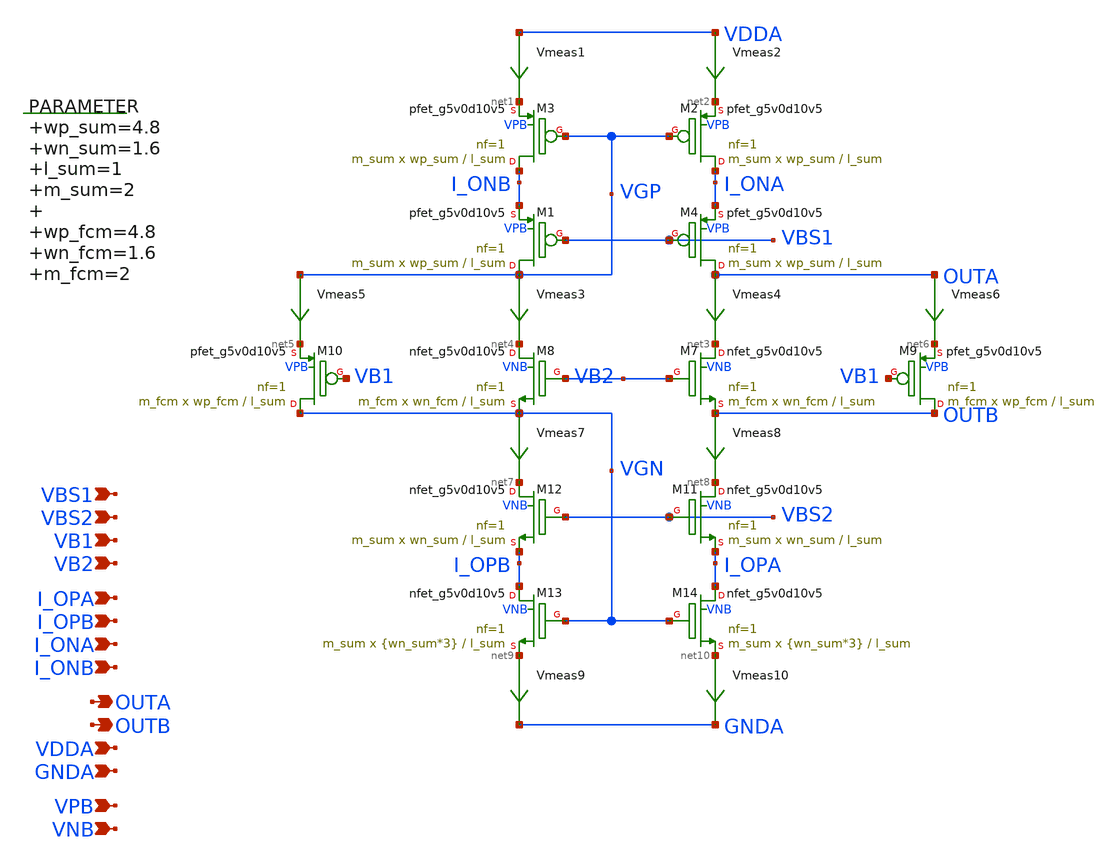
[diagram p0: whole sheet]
** sch_path: xschem/folded_cascode.sch
**.subckt folded_cascode I_OPA I_OPB I_ONA I_ONB OUTA OUTB VBS1 VBS2 VB1 VB2 VDDA VPB GNDA VNB
*.ipin I_OPA
*.ipin I_OPB
*.ipin I_ONA
*.ipin I_ONB
*.opin OUTA
*.opin OUTB
*.ipin VBS1
*.ipin VBS2
*.ipin VB1
*.ipin VB2
*.ipin VDDA
*.ipin VPB
*.ipin GNDA
*.ipin VNB
.param wp_sum=4.8 wn_sum=1.6 l_sum=1 m_sum=2 wp_fcm=4.8 wn_fcm=1.6 m_fcm=2

XM3 I_ONB VGP net1 VPB sky130_fd_pr__pfet_g5v0d10v5 L=l_sum W=wp_sum nf=1 ad='int((nf+1)/2) * W/nf * 0.29'
+ as='int((nf+2)/2) * W/nf * 0.29' pd='2*int((nf+1)/2) * (W/nf + 0.29)' ps='2*int((nf+2)/2) * (W/nf + 0.29)'
+ nrd='0.29 / W' nrs='0.29 / W' sa=0 sb=0 sd=0 mult=m_sum m=m_sum
Vmeas1 VDDA net1 0
.save i(vmeas1)
Vmeas2 VDDA net2 0
.save i(vmeas2)
XM7 net3 VB2 OUTB VNB sky130_fd_pr__nfet_g5v0d10v5 L=l_sum W=wn_fcm nf=1 ad='int((nf+1)/2) * W/nf * 0.29'
+ as='int((nf+2)/2) * W/nf * 0.29' pd='2*int((nf+1)/2) * (W/nf + 0.29)' ps='2*int((nf+2)/2) * (W/nf + 0.29)'
+ nrd='0.29 / W' nrs='0.29 / W' sa=0 sb=0 sd=0 mult=m_fcm m=m_fcm
XM8 net4 VB2 VGN VNB sky130_fd_pr__nfet_g5v0d10v5 L=l_sum W=wn_fcm nf=1 ad='int((nf+1)/2) * W/nf * 0.29'
+ as='int((nf+2)/2) * W/nf * 0.29' pd='2*int((nf+1)/2) * (W/nf + 0.29)' ps='2*int((nf+2)/2) * (W/nf + 0.29)'
+ nrd='0.29 / W' nrs='0.29 / W' sa=0 sb=0 sd=0 mult=m_fcm m=m_fcm
Vmeas3 VGP net4 0
.save i(vmeas3)
Vmeas4 OUTA net3 0
.save i(vmeas4)
XM10 VGN VB1 net5 VPB sky130_fd_pr__pfet_g5v0d10v5 L=l_sum W=wp_fcm nf=1 ad='int((nf+1)/2) * W/nf * 0.29'
+ as='int((nf+2)/2) * W/nf * 0.29' pd='2*int((nf+1)/2) * (W/nf + 0.29)' ps='2*int((nf+2)/2) * (W/nf + 0.29)'
+ nrd='0.29 / W' nrs='0.29 / W' sa=0 sb=0 sd=0 mult=m_fcm m=m_fcm
Vmeas5 VGP net5 0
.save i(vmeas5)
Vmeas6 OUTA net6 0
.save i(vmeas6)
XM9 OUTB VB1 net6 VPB sky130_fd_pr__pfet_g5v0d10v5 L=l_sum W=wp_fcm nf=1 ad='int((nf+1)/2) * W/nf * 0.29'
+ as='int((nf+2)/2) * W/nf * 0.29' pd='2*int((nf+1)/2) * (W/nf + 0.29)' ps='2*int((nf+2)/2) * (W/nf + 0.29)'
+ nrd='0.29 / W' nrs='0.29 / W' sa=0 sb=0 sd=0 mult=m_fcm m=m_fcm
XM12 net7 VBS2 I_OPB VNB sky130_fd_pr__nfet_g5v0d10v5 L=l_sum W=wn_sum nf=1 ad='int((nf+1)/2) * W/nf * 0.29'
+ as='int((nf+2)/2) * W/nf * 0.29' pd='2*int((nf+1)/2) * (W/nf + 0.29)' ps='2*int((nf+2)/2) * (W/nf + 0.29)'
+ nrd='0.29 / W' nrs='0.29 / W' sa=0 sb=0 sd=0 mult=m_sum m=m_sum
Vmeas7 VGN net7 0
.save i(vmeas7)
Vmeas8 OUTB net8 0
.save i(vmeas8)
XM11 net8 VBS2 I_OPA VNB sky130_fd_pr__nfet_g5v0d10v5 L=l_sum W=wn_sum nf=1 ad='int((nf+1)/2) * W/nf * 0.29'
+ as='int((nf+2)/2) * W/nf * 0.29' pd='2*int((nf+1)/2) * (W/nf + 0.29)' ps='2*int((nf+2)/2) * (W/nf + 0.29)'
+ nrd='0.29 / W' nrs='0.29 / W' sa=0 sb=0 sd=0 mult=m_sum m=m_sum
XM13 I_OPB VGN net9 VNB sky130_fd_pr__nfet_g5v0d10v5 L=l_sum W={wn_sum*3} nf=1 ad='int((nf+1)/2) * W/nf * 0.29'
+ as='int((nf+2)/2) * W/nf * 0.29' pd='2*int((nf+1)/2) * (W/nf + 0.29)' ps='2*int((nf+2)/2) * (W/nf + 0.29)'
+ nrd='0.29 / W' nrs='0.29 / W' sa=0 sb=0 sd=0 mult=m_sum m=m_sum
Vmeas9 net9 GNDA 0
.save i(vmeas9)
Vmeas10 net10 GNDA 0
.save i(vmeas10)
XM14 I_OPA VGN net10 VNB sky130_fd_pr__nfet_g5v0d10v5 L=l_sum W={wn_sum*3} nf=1 ad='int((nf+1)/2) * W/nf * 0.29'
+ as='int((nf+2)/2) * W/nf * 0.29' pd='2*int((nf+1)/2) * (W/nf + 0.29)' ps='2*int((nf+2)/2) * (W/nf + 0.29)'
+ nrd='0.29 / W' nrs='0.29 / W' sa=0 sb=0 sd=0 mult=m_sum m=m_sum
XM1 VGP VBS1 I_ONB VPB sky130_fd_pr__pfet_g5v0d10v5 L=l_sum W=wp_sum nf=1 ad='int((nf+1)/2) * W/nf * 0.29'
+ as='int((nf+2)/2) * W/nf * 0.29' pd='2*int((nf+1)/2) * (W/nf + 0.29)' ps='2*int((nf+2)/2) * (W/nf + 0.29)'
+ nrd='0.29 / W' nrs='0.29 / W' sa=0 sb=0 sd=0 mult=m_sum m=m_sum
XM2 I_ONA VGP net2 VPB sky130_fd_pr__pfet_g5v0d10v5 L=l_sum W=wp_sum nf=1 ad='int((nf+1)/2) * W/nf * 0.29'
+ as='int((nf+2)/2) * W/nf * 0.29' pd='2*int((nf+1)/2) * (W/nf + 0.29)' ps='2*int((nf+2)/2) * (W/nf + 0.29)'
+ nrd='0.29 / W' nrs='0.29 / W' sa=0 sb=0 sd=0 mult=m_sum m=m_sum
XM4 OUTA VBS1 I_ONA VPB sky130_fd_pr__pfet_g5v0d10v5 L=l_sum W=wp_sum nf=1 ad='int((nf+1)/2) * W/nf * 0.29'
+ as='int((nf+2)/2) * W/nf * 0.29' pd='2*int((nf+1)/2) * (W/nf + 0.29)' ps='2*int((nf+2)/2) * (W/nf + 0.29)'
+ nrd='0.29 / W' nrs='0.29 / W' sa=0 sb=0 sd=0 mult=m_sum m=m_sum
**.ends
.end
